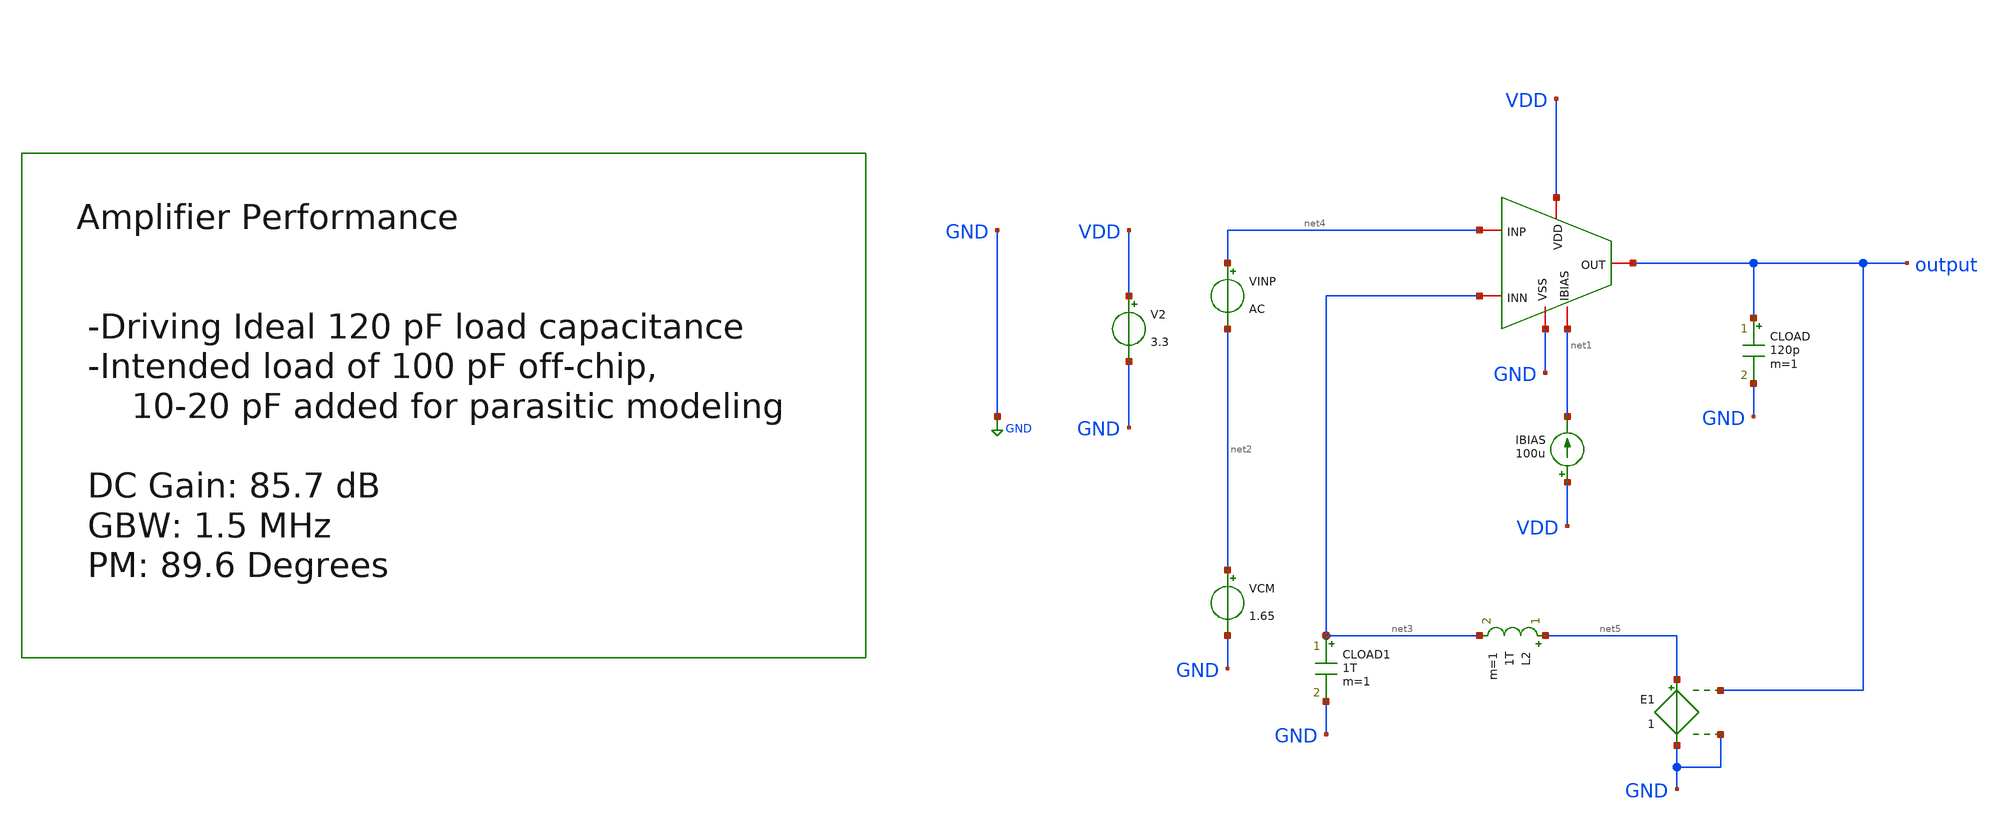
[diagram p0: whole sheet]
** sch_path: designs/libs/core_amps/ota_folded_cascode/tb/open_loop_ac_tb.sch
**.subckt open_loop_ac_tb
IBIAS VDD net1 100u
V2 VDD GND 3.3
CLOAD output GND 120p m=1
VINP net4 net2 AC
VCM net2 GND 1.65
L2 net5 net3 1T m=1
CLOAD1 net3 GND 1T m=1
E1 net5 GND output GND 1
x1 VDD GND output net4 net3 net1 ota_folded_cascode
**** begin user architecture code

.include $::180MCU_MODELS/design.ngspice
.lib $::180MCU_MODELS/sm141064.ngspice typical



.control

set color0=white
set color1=black
set color2=red
set color3=blue

ac dec 100 1 1G

plot vdb(output) ph(v(output))*180/3.14159

meas ac dc_gain find vdb(output) at=1
meas ac gbw when vdb(output)=0
let gain_db = vdb(output)
let phase = 180/3.14159*ph(v(output))
meas ac phase_at_gbw find phase when vdb(output)=0
let pm = 180 + phase_at_gbw
print pm

.endc



**** end user architecture code
**.ends
.GLOBAL GND
.end
